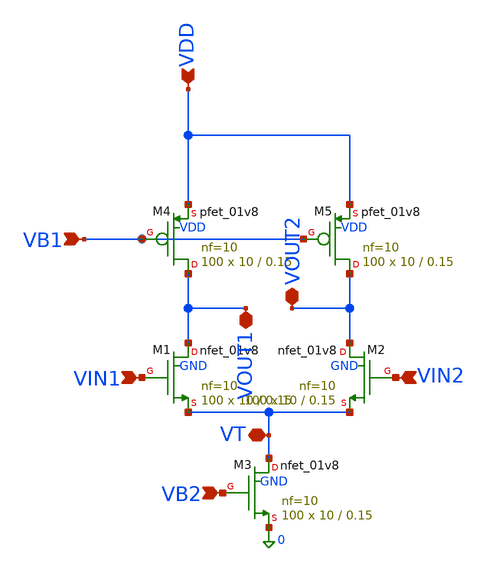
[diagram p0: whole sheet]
** sch_path: MOS-Circuits/Differential Pair/Diff_Pair_1/diff_pair_load1.sch
**.subckt diff_pair_load1 VOUT1 VOUT2 VIN1 VIN2 VB2 VDD VB1 VT
*.iopin VOUT1
*.iopin VOUT2
*.ipin VIN1
*.ipin VIN2
*.ipin VB2
*.ipin VDD
*.ipin VB1
*.iopin VT
XM1 VOUT1 VIN1 VT GND sky130_fd_pr__nfet_01v8 L=0.15 W=10 nf=10 ad='int((nf+1)/2) * W/nf * 0.29' as='int((nf+2)/2) * W/nf * 0.29'
+ pd='2*int((nf+1)/2) * (W/nf + 0.29)' ps='2*int((nf+2)/2) * (W/nf + 0.29)' nrd='0.29 / W' nrs='0.29 / W'
+ sa=0 sb=0 sd=0 mult=100 m=100
XM2 VOUT2 VIN2 VT GND sky130_fd_pr__nfet_01v8 L=0.15 W=10 nf=10 ad='int((nf+1)/2) * W/nf * 0.29' as='int((nf+2)/2) * W/nf * 0.29'
+ pd='2*int((nf+1)/2) * (W/nf + 0.29)' ps='2*int((nf+2)/2) * (W/nf + 0.29)' nrd='0.29 / W' nrs='0.29 / W'
+ sa=0 sb=0 sd=0 mult=100 m=100
XM3 VT VB2 0 GND sky130_fd_pr__nfet_01v8 L=0.15 W=10 nf=10 ad='int((nf+1)/2) * W/nf * 0.29' as='int((nf+2)/2) * W/nf * 0.29'
+ pd='2*int((nf+1)/2) * (W/nf + 0.29)' ps='2*int((nf+2)/2) * (W/nf + 0.29)' nrd='0.29 / W' nrs='0.29 / W'
+ sa=0 sb=0 sd=0 mult=100 m=100
XM4 VOUT1 VB1 VDD VDD sky130_fd_pr__pfet_01v8 L=0.15 W=10 nf=10 ad='int((nf+1)/2) * W/nf * 0.29' as='int((nf+2)/2) * W/nf * 0.29'
+ pd='2*int((nf+1)/2) * (W/nf + 0.29)' ps='2*int((nf+2)/2) * (W/nf + 0.29)' nrd='0.29 / W' nrs='0.29 / W'
+ sa=0 sb=0 sd=0 mult=100 m=100
XM5 VOUT2 VB1 VDD VDD sky130_fd_pr__pfet_01v8 L=0.15 W=10 nf=10 ad='int((nf+1)/2) * W/nf * 0.29' as='int((nf+2)/2) * W/nf * 0.29'
+ pd='2*int((nf+1)/2) * (W/nf + 0.29)' ps='2*int((nf+2)/2) * (W/nf + 0.29)' nrd='0.29 / W' nrs='0.29 / W'
+ sa=0 sb=0 sd=0 mult=100 m=100
**.ends
.end
